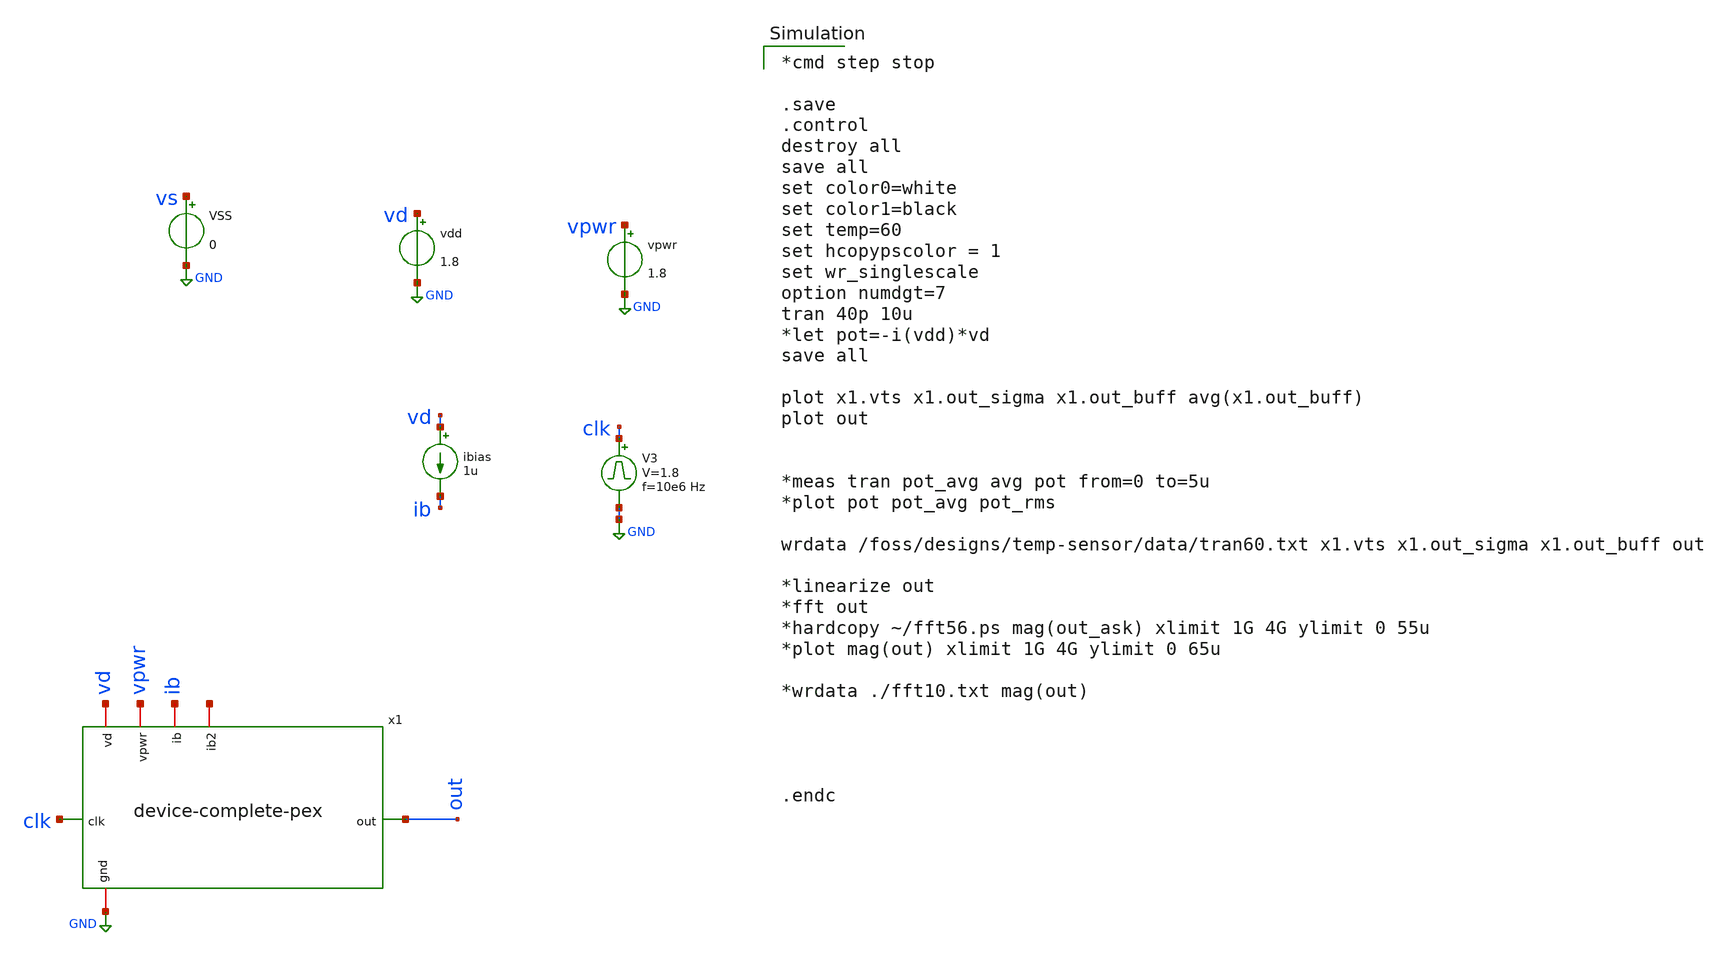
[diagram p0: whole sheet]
** sch_path: device-complete/xschem/device-complete-tb.sch
**.subckt device-complete-tb
vpwr vpwr GND 1.8
V3 clk GND pulse 0 1.8 '0.495/ 10e6 ' '0.01/10e6 ' '0.01/10e6 ' '0.49/10e6 ' '1/10e6 '
vdd vd GND 1.8
ibias vd ib 1u
VSS vs GND 0
x1 vd clk out vpwr ib net1 GND device-complete-pex
**** begin user architecture code

*cmd step stop

.save
.control
destroy all
save all
set color0=white
set color1=black
set temp=60
set hcopypscolor = 1
set wr_singlescale
option numdgt=7
tran 40p 10u
*let pot=-i(vdd)*vd
save all

plot x1.vts x1.out_sigma x1.out_buff avg(x1.out_buff)
plot out


*meas tran pot_avg avg pot from=0 to=5u
*plot pot pot_avg pot_rms

wrdata /foss/designs/temp-sensor/data/tran60.txt x1.vts x1.out_sigma x1.out_buff out

*linearize out
*fft out
*hardcopy ~/fft56.ps mag(out_ask) xlimit 1G 4G ylimit 0 55u
*plot mag(out) xlimit 1G 4G ylimit 0 65u

*wrdata ./fft10.txt mag(out)




.endc



 .lib $::SKYWATER_MODELS/sky130.lib.spice tt
.include $::SKYWATER_STDCELLS/sky130_fd_sc_hd.spice

**** end user architecture code
**.ends
.GLOBAL GND
.end
